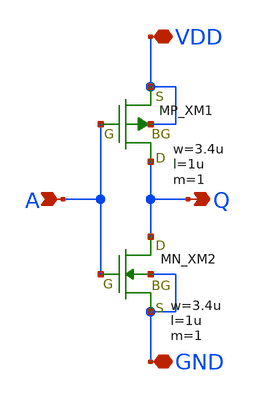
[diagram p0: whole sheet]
** sch_path: inverter/inverter.sch
**.subckt inverter A Q VDD GND
*.ipin A
*.opin Q
*.iopin VDD
*.iopin GND
XXM1 Q A VDD VDD PMOS w=3.4u l=1u nrd=0 nrs=0 m=1
XXM2 Q A GND GND NMOS w=3.4u l=1u nrd=0 nrs=0 m=1
**.ends
.end
